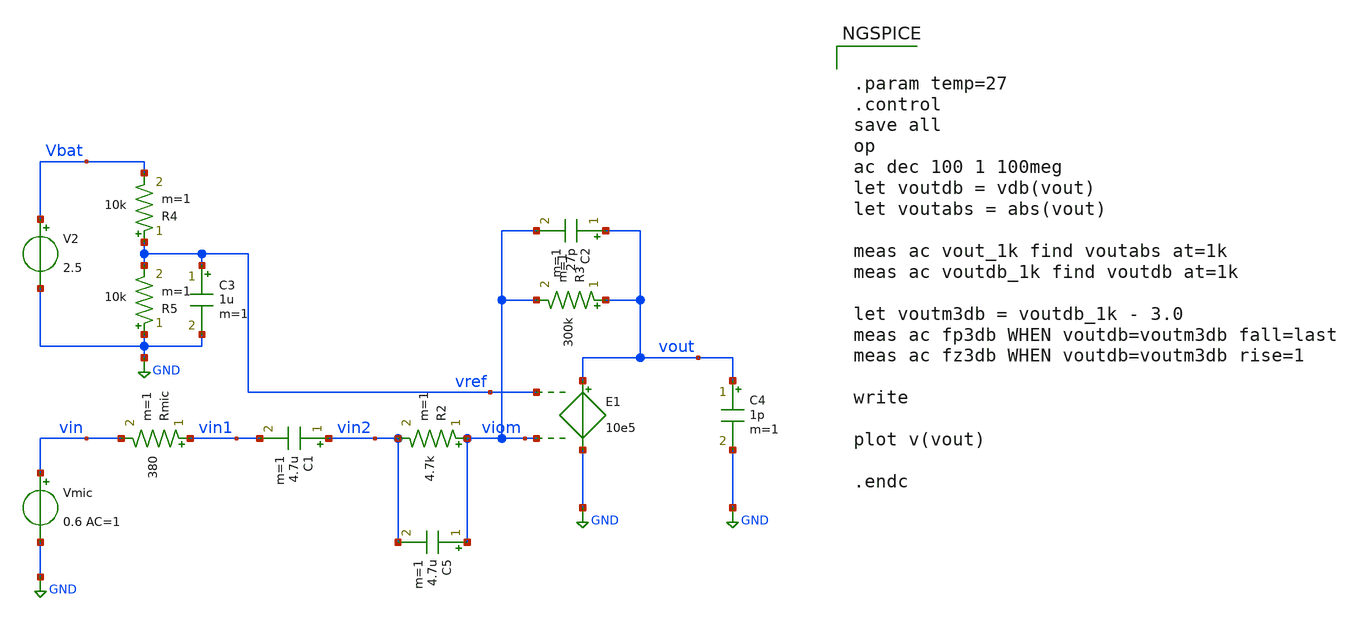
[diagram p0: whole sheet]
** sch_path: xschem/TB_mic_pole.sch
**.subckt TB_mic_pole
Vmic vin GND 0.6 AC=1
Rmic vin1 vin 380 m=1
C1 vin2 vin1 4.7u m=1
R2 viom vin2 4.7k m=1
E1 vout GND vref viom 10e5
V2 Vbat GND 2.5
R3 vout viom 300k m=1
C2 vout viom 27p m=1
R4 vref Vbat 10k m=1
R5 GND vref 10k m=1
C3 vref GND 1u m=1
C4 vout GND 1p m=1
C5 viom vin2 4.7u m=1
**** begin user architecture code


.param temp=27
.control
save all
op
ac dec 100 1 100meg
let voutdb = vdb(vout)
let voutabs = abs(vout)

meas ac vout_1k find voutabs at=1k
meas ac voutdb_1k find voutdb at=1k

let voutm3db = voutdb_1k - 3.0
meas ac fp3db WHEN voutdb=voutm3db fall=last
meas ac fz3db WHEN voutdb=voutm3db rise=1

write

plot v(vout)

.endc


**** end user architecture code
**.ends
.GLOBAL GND
.end
